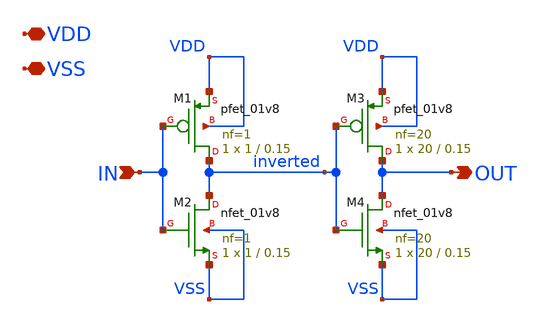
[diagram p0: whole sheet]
** sch_path: xschem/double_inverter.sch
**.subckt double_inverter VDD VSS IN OUT
*.iopin VDD
*.iopin VSS
*.ipin IN
*.opin OUT
XM1 inverted IN VDD VDD sky130_fd_pr__pfet_01v8 L=0.15 W=1 nf=1 ad='int((nf+1)/2) * W/nf * 0.29' as='int((nf+2)/2) * W/nf * 0.29'
+ pd='2*int((nf+1)/2) * (W/nf + 0.29)' ps='2*int((nf+2)/2) * (W/nf + 0.29)' nrd='0.29 / W' nrs='0.29 / W'
+ sa=0 sb=0 sd=0 mult=1 m=1
XM2 inverted IN VSS VSS sky130_fd_pr__nfet_01v8 L=0.15 W=1 nf=1 ad='int((nf+1)/2) * W/nf * 0.29' as='int((nf+2)/2) * W/nf * 0.29'
+ pd='2*int((nf+1)/2) * (W/nf + 0.29)' ps='2*int((nf+2)/2) * (W/nf + 0.29)' nrd='0.29 / W' nrs='0.29 / W'
+ sa=0 sb=0 sd=0 mult=1 m=1
XM3 OUT inverted VDD VDD sky130_fd_pr__pfet_01v8 L=0.15 W=20 nf=20 ad='int((nf+1)/2) * W/nf * 0.29' as='int((nf+2)/2) * W/nf * 0.29'
+ pd='2*int((nf+1)/2) * (W/nf + 0.29)' ps='2*int((nf+2)/2) * (W/nf + 0.29)' nrd='0.29 / W' nrs='0.29 / W'
+ sa=0 sb=0 sd=0 mult=1 m=1
XM4 OUT inverted VSS VSS sky130_fd_pr__nfet_01v8 L=0.15 W=20 nf=20 ad='int((nf+1)/2) * W/nf * 0.29' as='int((nf+2)/2) * W/nf * 0.29'
+ pd='2*int((nf+1)/2) * (W/nf + 0.29)' ps='2*int((nf+2)/2) * (W/nf + 0.29)' nrd='0.29 / W' nrs='0.29 / W'
+ sa=0 sb=0 sd=0 mult=1 m=1
**.ends
.end
